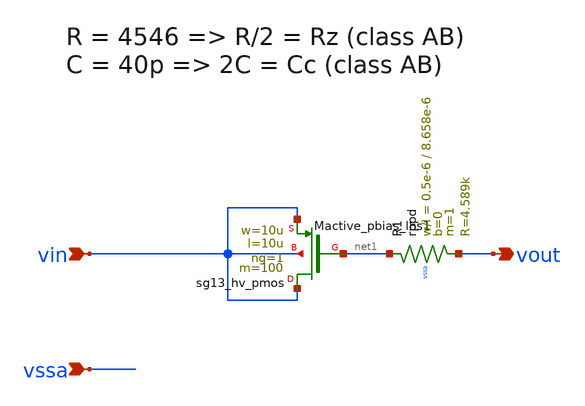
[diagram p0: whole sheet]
** sch_path: Schematics_Layout/sunrise_opamp_pcomp/sunrise_opamp_pcomp.sch
**.subckt sunrise_opamp_pcomp vssa vout vin
*.ipin vssa
*.opin vout
*.ipin vin
XMactive_pbias_lhs1 vin net1 vin vin sg13_hv_pmos w=10u l=10u ng=1 m=100 mm_ok=1
XR1 net1 vout vssa rppd w=0.5e-6 l=8.658e-6 m=1 b=0 mm_ok=1
**.ends
.end
